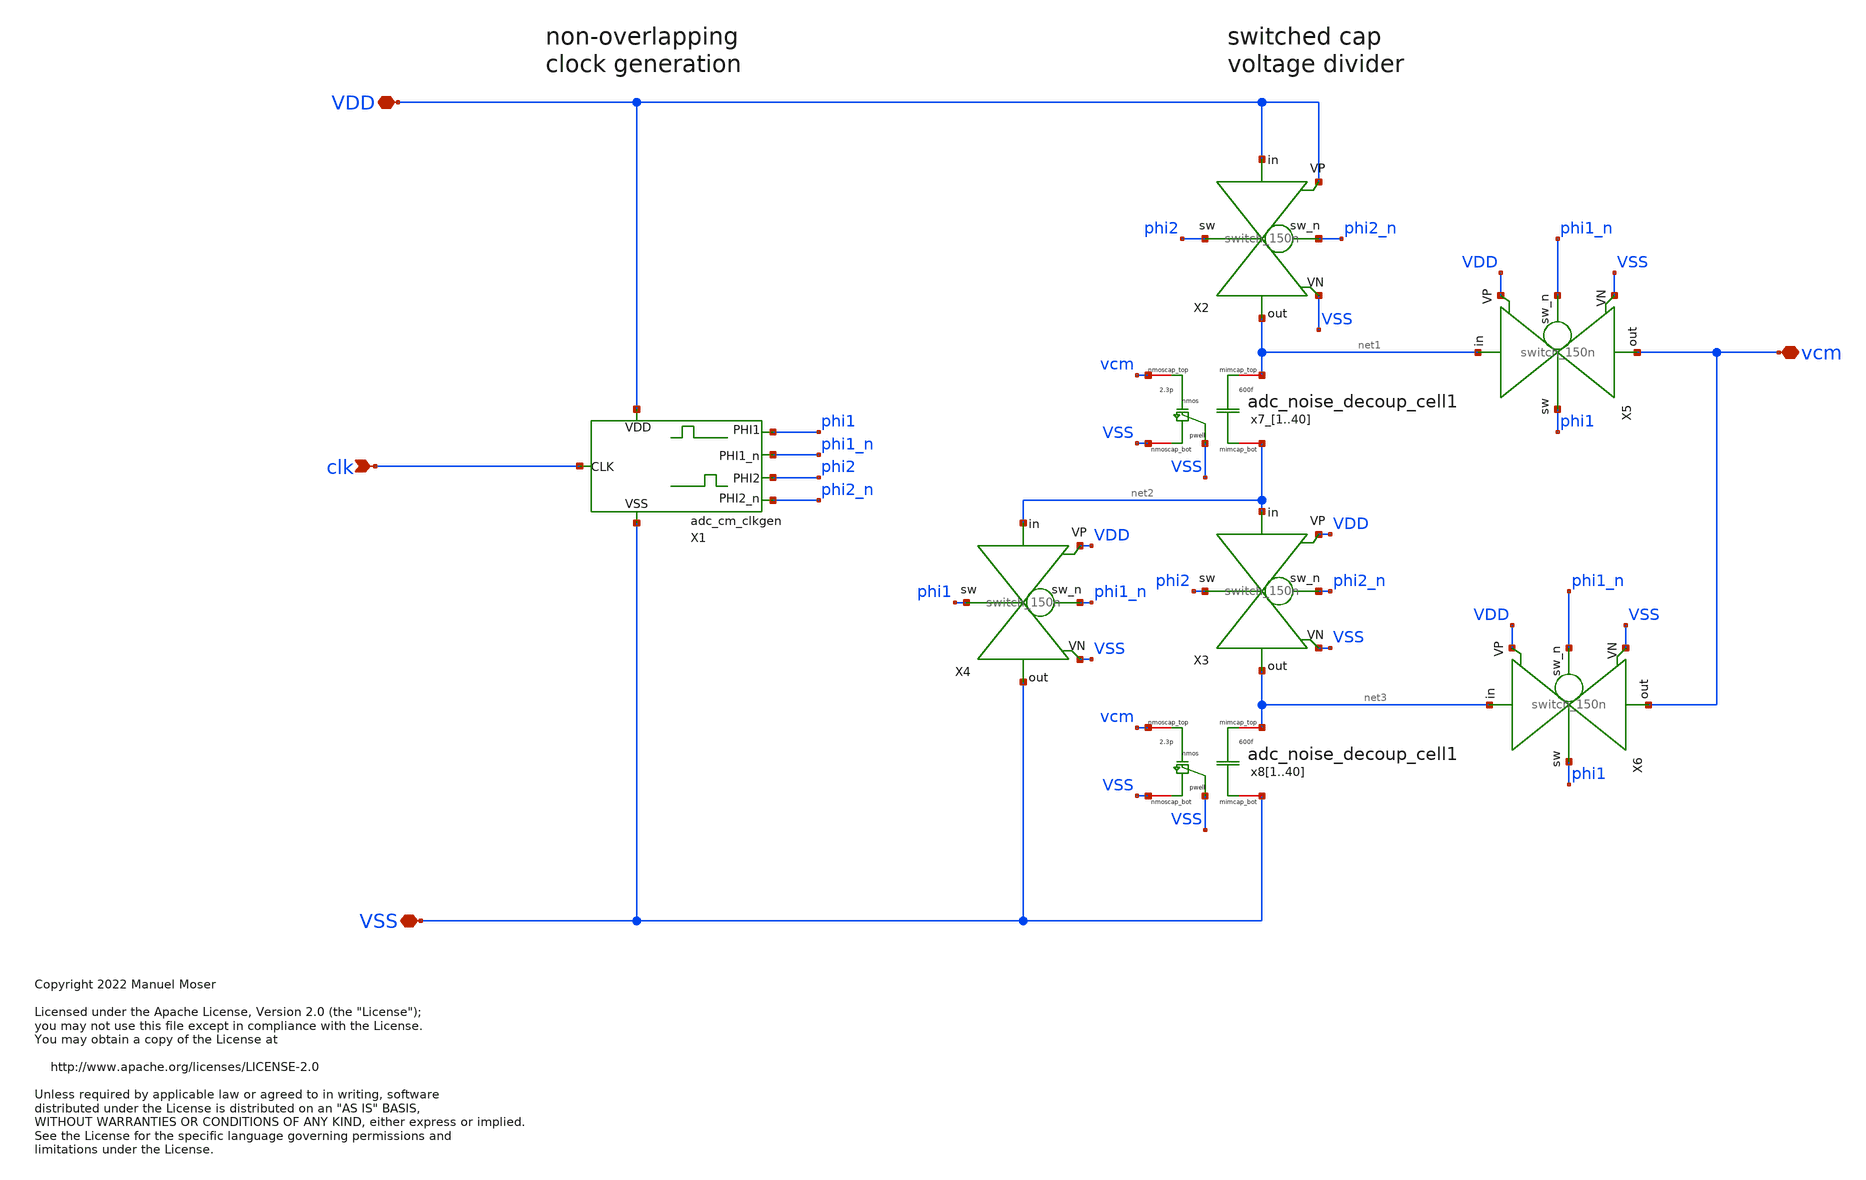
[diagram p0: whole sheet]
** sch_path: xschem/adc_vcm_gen/adc_vcm_gen.sch
* Copyright 2022 Manuel Moser
* Licensed under the Apache License, Version 2.0 (the "License");
**.subckt adc_vcm_gen VDD VSS clk vcm
*.iopin VDD
*.iopin VSS
*.ipin clk
*.iopin vcm
X1 clk VDD VSS phi1_n phi1 phi2 phi2_n adc_cm_clkgen
X2 phi2_n VDD phi2 net1 VDD VSS switch_150n
X3 phi2_n net2 phi2 net3 VDD VSS switch_150n
X4 phi1_n net2 phi1 VSS VDD VSS switch_150n
X5 phi1_n net1 phi1 vcm VDD VSS switch_150n
X6 phi1_n net3 phi1 vcm VDD VSS switch_150n
x7_1 net1 net2 vcm VSS VSS adc_noise_decoup_cell1
x7_2 net1 net2 vcm VSS VSS adc_noise_decoup_cell1
x7_3 net1 net2 vcm VSS VSS adc_noise_decoup_cell1
x7_4 net1 net2 vcm VSS VSS adc_noise_decoup_cell1
x7_5 net1 net2 vcm VSS VSS adc_noise_decoup_cell1
x7_6 net1 net2 vcm VSS VSS adc_noise_decoup_cell1
x7_7 net1 net2 vcm VSS VSS adc_noise_decoup_cell1
x7_8 net1 net2 vcm VSS VSS adc_noise_decoup_cell1
x7_9 net1 net2 vcm VSS VSS adc_noise_decoup_cell1
x7_10 net1 net2 vcm VSS VSS adc_noise_decoup_cell1
x7_11 net1 net2 vcm VSS VSS adc_noise_decoup_cell1
x7_12 net1 net2 vcm VSS VSS adc_noise_decoup_cell1
x7_13 net1 net2 vcm VSS VSS adc_noise_decoup_cell1
x7_14 net1 net2 vcm VSS VSS adc_noise_decoup_cell1
x7_15 net1 net2 vcm VSS VSS adc_noise_decoup_cell1
x7_16 net1 net2 vcm VSS VSS adc_noise_decoup_cell1
x7_17 net1 net2 vcm VSS VSS adc_noise_decoup_cell1
x7_18 net1 net2 vcm VSS VSS adc_noise_decoup_cell1
x7_19 net1 net2 vcm VSS VSS adc_noise_decoup_cell1
x7_20 net1 net2 vcm VSS VSS adc_noise_decoup_cell1
x7_21 net1 net2 vcm VSS VSS adc_noise_decoup_cell1
x7_22 net1 net2 vcm VSS VSS adc_noise_decoup_cell1
x7_23 net1 net2 vcm VSS VSS adc_noise_decoup_cell1
x7_24 net1 net2 vcm VSS VSS adc_noise_decoup_cell1
x7_25 net1 net2 vcm VSS VSS adc_noise_decoup_cell1
x7_26 net1 net2 vcm VSS VSS adc_noise_decoup_cell1
x7_27 net1 net2 vcm VSS VSS adc_noise_decoup_cell1
x7_28 net1 net2 vcm VSS VSS adc_noise_decoup_cell1
x7_29 net1 net2 vcm VSS VSS adc_noise_decoup_cell1
x7_30 net1 net2 vcm VSS VSS adc_noise_decoup_cell1
x7_31 net1 net2 vcm VSS VSS adc_noise_decoup_cell1
x7_32 net1 net2 vcm VSS VSS adc_noise_decoup_cell1
x7_33 net1 net2 vcm VSS VSS adc_noise_decoup_cell1
x7_34 net1 net2 vcm VSS VSS adc_noise_decoup_cell1
x7_35 net1 net2 vcm VSS VSS adc_noise_decoup_cell1
x7_36 net1 net2 vcm VSS VSS adc_noise_decoup_cell1
x7_37 net1 net2 vcm VSS VSS adc_noise_decoup_cell1
x7_38 net1 net2 vcm VSS VSS adc_noise_decoup_cell1
x7_39 net1 net2 vcm VSS VSS adc_noise_decoup_cell1
x7_40 net1 net2 vcm VSS VSS adc_noise_decoup_cell1
x81 net3 VSS vcm VSS VSS adc_noise_decoup_cell1
x82 net3 VSS vcm VSS VSS adc_noise_decoup_cell1
x83 net3 VSS vcm VSS VSS adc_noise_decoup_cell1
x84 net3 VSS vcm VSS VSS adc_noise_decoup_cell1
x85 net3 VSS vcm VSS VSS adc_noise_decoup_cell1
x86 net3 VSS vcm VSS VSS adc_noise_decoup_cell1
x87 net3 VSS vcm VSS VSS adc_noise_decoup_cell1
x88 net3 VSS vcm VSS VSS adc_noise_decoup_cell1
x89 net3 VSS vcm VSS VSS adc_noise_decoup_cell1
x810 net3 VSS vcm VSS VSS adc_noise_decoup_cell1
x811 net3 VSS vcm VSS VSS adc_noise_decoup_cell1
x812 net3 VSS vcm VSS VSS adc_noise_decoup_cell1
x813 net3 VSS vcm VSS VSS adc_noise_decoup_cell1
x814 net3 VSS vcm VSS VSS adc_noise_decoup_cell1
x815 net3 VSS vcm VSS VSS adc_noise_decoup_cell1
x816 net3 VSS vcm VSS VSS adc_noise_decoup_cell1
x817 net3 VSS vcm VSS VSS adc_noise_decoup_cell1
x818 net3 VSS vcm VSS VSS adc_noise_decoup_cell1
x819 net3 VSS vcm VSS VSS adc_noise_decoup_cell1
x820 net3 VSS vcm VSS VSS adc_noise_decoup_cell1
x821 net3 VSS vcm VSS VSS adc_noise_decoup_cell1
x822 net3 VSS vcm VSS VSS adc_noise_decoup_cell1
x823 net3 VSS vcm VSS VSS adc_noise_decoup_cell1
x824 net3 VSS vcm VSS VSS adc_noise_decoup_cell1
x825 net3 VSS vcm VSS VSS adc_noise_decoup_cell1
x826 net3 VSS vcm VSS VSS adc_noise_decoup_cell1
x827 net3 VSS vcm VSS VSS adc_noise_decoup_cell1
x828 net3 VSS vcm VSS VSS adc_noise_decoup_cell1
x829 net3 VSS vcm VSS VSS adc_noise_decoup_cell1
x830 net3 VSS vcm VSS VSS adc_noise_decoup_cell1
x831 net3 VSS vcm VSS VSS adc_noise_decoup_cell1
x832 net3 VSS vcm VSS VSS adc_noise_decoup_cell1
x833 net3 VSS vcm VSS VSS adc_noise_decoup_cell1
x834 net3 VSS vcm VSS VSS adc_noise_decoup_cell1
x835 net3 VSS vcm VSS VSS adc_noise_decoup_cell1
x836 net3 VSS vcm VSS VSS adc_noise_decoup_cell1
x837 net3 VSS vcm VSS VSS adc_noise_decoup_cell1
x838 net3 VSS vcm VSS VSS adc_noise_decoup_cell1
x839 net3 VSS vcm VSS VSS adc_noise_decoup_cell1
x840 net3 VSS vcm VSS VSS adc_noise_decoup_cell1
**.ends
.end
